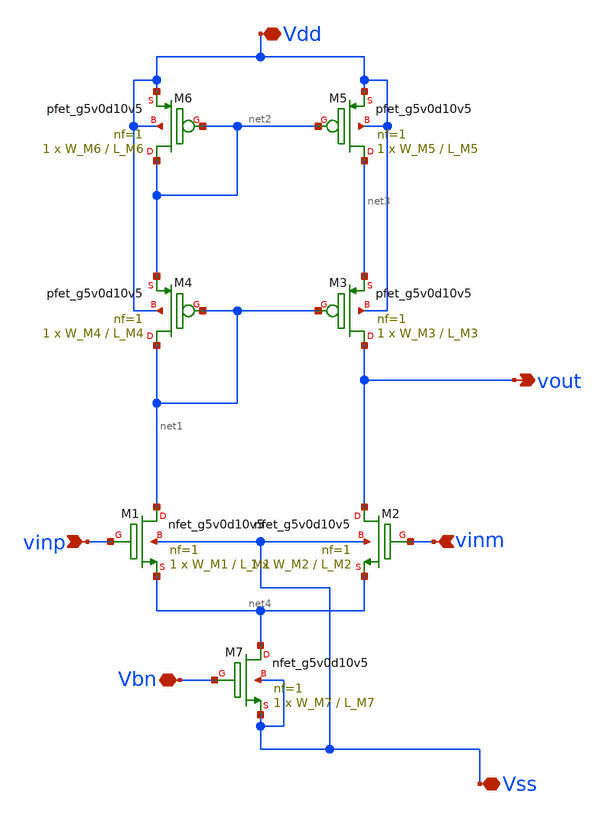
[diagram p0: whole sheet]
** sch_path: xschem/diff_pair_cascode.sch
**.subckt diff_pair_cascode vinm vinp Vbn vout Vss Vdd
*.ipin vinm
*.ipin vinp
*.iopin Vbn
*.opin vout
*.iopin Vss
*.iopin Vdd
XM1 net1 vinp net4 Vss sky130_fd_pr__nfet_g5v0d10v5 L=L_M1 W=W_M1 nf=1 ad='int((nf+1)/2) * W/nf * 0.29'
+ as='int((nf+2)/2) * W/nf * 0.29' pd='2*int((nf+1)/2) * (W/nf + 0.29)' ps='2*int((nf+2)/2) * (W/nf + 0.29)'
+ nrd='0.29 / W' nrs='0.29 / W' sa=0 sb=0 sd=0 mult=1 m=1
XM2 vout vinm net4 Vss sky130_fd_pr__nfet_g5v0d10v5 L=L_M2 W=W_M2 nf=1 ad='int((nf+1)/2) * W/nf * 0.29'
+ as='int((nf+2)/2) * W/nf * 0.29' pd='2*int((nf+1)/2) * (W/nf + 0.29)' ps='2*int((nf+2)/2) * (W/nf + 0.29)'
+ nrd='0.29 / W' nrs='0.29 / W' sa=0 sb=0 sd=0 mult=1 m=1
XM3 vout net1 net3 Vdd sky130_fd_pr__pfet_g5v0d10v5 L=L_M3 W=W_M3 nf=1 ad='int((nf+1)/2) * W/nf * 0.29'
+ as='int((nf+2)/2) * W/nf * 0.29' pd='2*int((nf+1)/2) * (W/nf + 0.29)' ps='2*int((nf+2)/2) * (W/nf + 0.29)'
+ nrd='0.29 / W' nrs='0.29 / W' sa=0 sb=0 sd=0 mult=1 m=1
XM4 net1 net1 net2 Vdd sky130_fd_pr__pfet_g5v0d10v5 L=L_M4 W=W_M4 nf=1 ad='int((nf+1)/2) * W/nf * 0.29'
+ as='int((nf+2)/2) * W/nf * 0.29' pd='2*int((nf+1)/2) * (W/nf + 0.29)' ps='2*int((nf+2)/2) * (W/nf + 0.29)'
+ nrd='0.29 / W' nrs='0.29 / W' sa=0 sb=0 sd=0 mult=1 m=1
XM7 net4 Vbn Vss Vss sky130_fd_pr__nfet_g5v0d10v5 L=L_M7 W=W_M7 nf=1 ad='int((nf+1)/2) * W/nf * 0.29'
+ as='int((nf+2)/2) * W/nf * 0.29' pd='2*int((nf+1)/2) * (W/nf + 0.29)' ps='2*int((nf+2)/2) * (W/nf + 0.29)'
+ nrd='0.29 / W' nrs='0.29 / W' sa=0 sb=0 sd=0 mult=1 m=1
XM5 net3 net2 Vdd Vdd sky130_fd_pr__pfet_g5v0d10v5 L=L_M5 W=W_M5 nf=1 ad='int((nf+1)/2) * W/nf * 0.29'
+ as='int((nf+2)/2) * W/nf * 0.29' pd='2*int((nf+1)/2) * (W/nf + 0.29)' ps='2*int((nf+2)/2) * (W/nf + 0.29)'
+ nrd='0.29 / W' nrs='0.29 / W' sa=0 sb=0 sd=0 mult=1 m=1
XM6 net2 net2 Vdd Vdd sky130_fd_pr__pfet_g5v0d10v5 L=L_M6 W=W_M6 nf=1 ad='int((nf+1)/2) * W/nf * 0.29'
+ as='int((nf+2)/2) * W/nf * 0.29' pd='2*int((nf+1)/2) * (W/nf + 0.29)' ps='2*int((nf+2)/2) * (W/nf + 0.29)'
+ nrd='0.29 / W' nrs='0.29 / W' sa=0 sb=0 sd=0 mult=1 m=1
**.ends
.end
